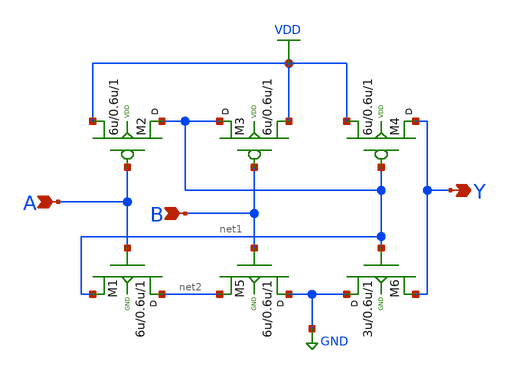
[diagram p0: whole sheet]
** sch_path: sch/AND2_1a.sch
**.subckt AND2_1a A B Y
*.ipin A
*.ipin B
*.opin Y
M1 net2 A net1 GND nfet w=6u l=0.6u m=1
M2 net1 A VDD VDD pfet w=6u l=0.6u m=1
M3 net1 B VDD VDD pfet w=6u l=0.6u m=1
M4 Y net1 VDD VDD pfet w=6u l=0.6u m=1
M5 GND B net2 GND nfet w=6u l=0.6u m=1
M6 GND net1 Y GND nfet w=3u l=0.6u m=1
**.ends
.GLOBAL GND
.GLOBAL VDD
.end
